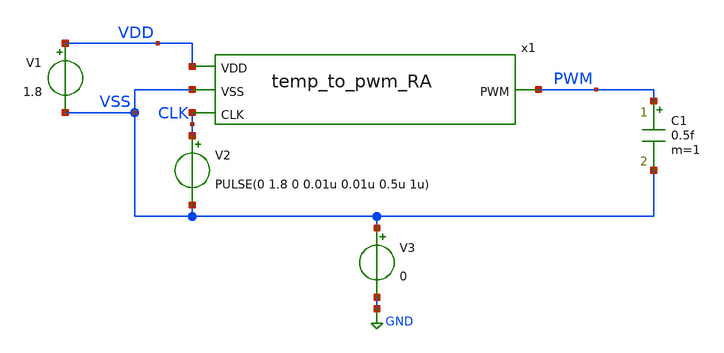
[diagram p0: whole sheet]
** sch_path: design/JNW_GR07_SKY130A/temp_to_pwm_RA_TB.sch
**.subckt temp_to_pwm_RA_TB
x1 VDD VSS PWM CLK temp_to_pwm_RA
V1 VDD VSS 1.8
V3 VSS GND 0
C1 PWM VSS 0.5f m=1
V2 CLK VSS PULSE(0 1.8 0 0.01u 0.01u 0.5u 1u)
**** begin user architecture code



.param mc_mm_switch=0
.param mc_pr_switch=0
.include ~/pro/aicex/ip/jnw_sv_sky130a/design/JNW_SV_SKY130A/simulation/tt.spi
* Options:
.option savecurrents
.option gmin=1e-15
.option temp=80
.save all
.control
tran 0.01u 20u
write temp_to_pwm_RA_TB.raw
*exit
.endc
.end



**** end user architecture code
**.ends
.GLOBAL GND
.end
